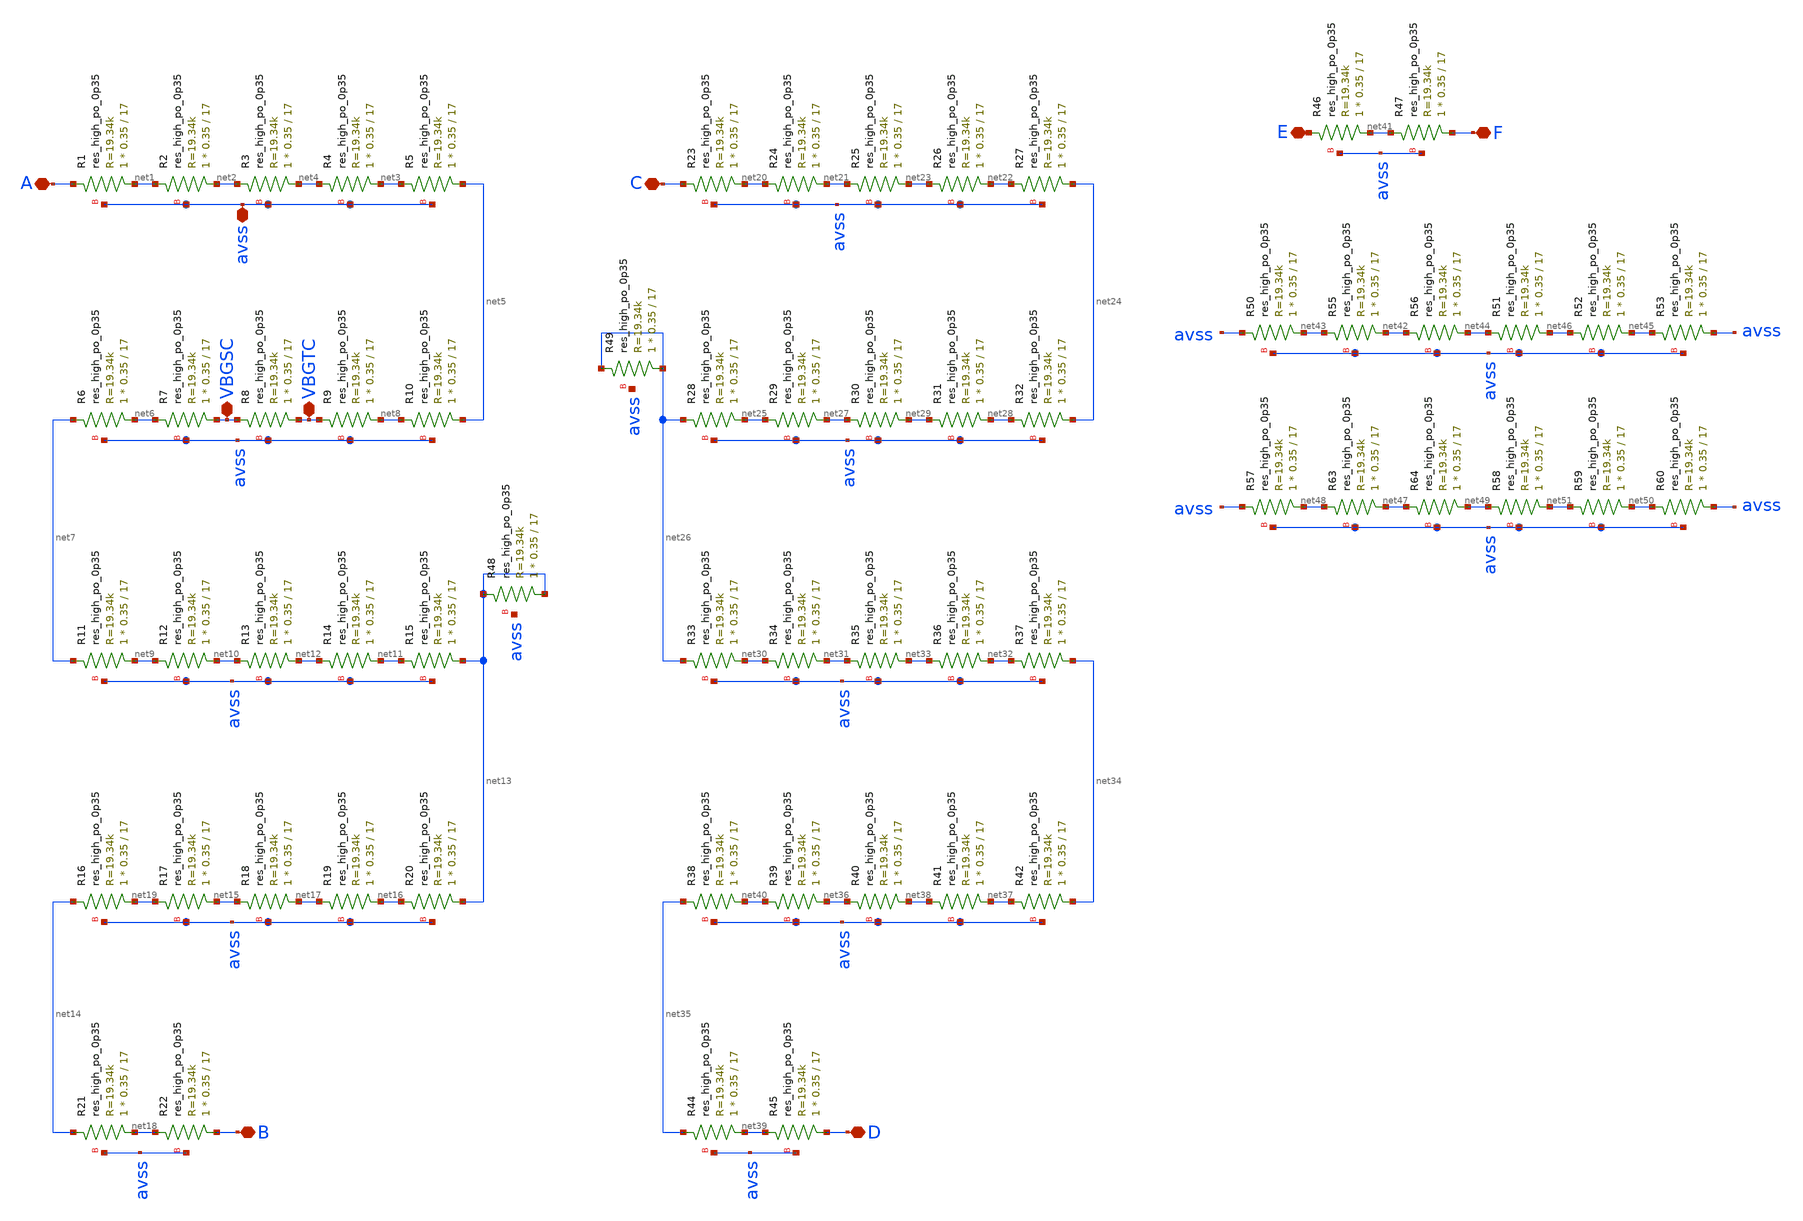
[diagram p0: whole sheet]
** sch_path: magic/resist_const.sch
**.subckt resist_const A VBGTC B VBGSC avss C D F E
*.iopin A
*.iopin VBGTC
*.iopin B
*.iopin VBGSC
*.iopin avss
*.iopin C
*.iopin D
*.iopin F
*.iopin E
XR1 net1 A avss sky130_fd_pr__res_high_po_0p35 L=17 mult=1 m=1
XR2 net2 net1 avss sky130_fd_pr__res_high_po_0p35 L=17 mult=1 m=1
XR3 net4 net2 avss sky130_fd_pr__res_high_po_0p35 L=17 mult=1 m=1
XR4 net3 net4 avss sky130_fd_pr__res_high_po_0p35 L=17 mult=1 m=1
XR5 net5 net3 avss sky130_fd_pr__res_high_po_0p35 L=17 mult=1 m=1
XR8 VBGTC VBGSC avss sky130_fd_pr__res_high_po_0p35 L=17 mult=1 m=1
XR9 net8 VBGTC avss sky130_fd_pr__res_high_po_0p35 L=17 mult=1 m=1
XR10 net5 net8 avss sky130_fd_pr__res_high_po_0p35 L=17 mult=1 m=1
XR12 net10 net9 avss sky130_fd_pr__res_high_po_0p35 L=17 mult=1 m=1
XR13 net12 net10 avss sky130_fd_pr__res_high_po_0p35 L=17 mult=1 m=1
XR14 net11 net12 avss sky130_fd_pr__res_high_po_0p35 L=17 mult=1 m=1
XR15 net13 net11 avss sky130_fd_pr__res_high_po_0p35 L=17 mult=1 m=1
XR17 net15 net19 avss sky130_fd_pr__res_high_po_0p35 L=17 mult=1 m=1
XR18 net17 net15 avss sky130_fd_pr__res_high_po_0p35 L=17 mult=1 m=1
XR19 net16 net17 avss sky130_fd_pr__res_high_po_0p35 L=17 mult=1 m=1
XR20 net13 net16 avss sky130_fd_pr__res_high_po_0p35 L=17 mult=1 m=1
XR22 B net18 avss sky130_fd_pr__res_high_po_0p35 L=17 mult=1 m=1
XR23 net20 C avss sky130_fd_pr__res_high_po_0p35 L=17 mult=1 m=1
XR24 net21 net20 avss sky130_fd_pr__res_high_po_0p35 L=17 mult=1 m=1
XR25 net23 net21 avss sky130_fd_pr__res_high_po_0p35 L=17 mult=1 m=1
XR26 net22 net23 avss sky130_fd_pr__res_high_po_0p35 L=17 mult=1 m=1
XR27 net24 net22 avss sky130_fd_pr__res_high_po_0p35 L=17 mult=1 m=1
XR30 net29 net27 avss sky130_fd_pr__res_high_po_0p35 L=17 mult=1 m=1
XR31 net28 net29 avss sky130_fd_pr__res_high_po_0p35 L=17 mult=1 m=1
XR32 net24 net28 avss sky130_fd_pr__res_high_po_0p35 L=17 mult=1 m=1
XR33 net30 net26 avss sky130_fd_pr__res_high_po_0p35 L=17 mult=1 m=1
XR34 net31 net30 avss sky130_fd_pr__res_high_po_0p35 L=17 mult=1 m=1
XR35 net33 net31 avss sky130_fd_pr__res_high_po_0p35 L=17 mult=1 m=1
XR36 net32 net33 avss sky130_fd_pr__res_high_po_0p35 L=17 mult=1 m=1
XR37 net34 net32 avss sky130_fd_pr__res_high_po_0p35 L=17 mult=1 m=1
XR39 net36 net40 avss sky130_fd_pr__res_high_po_0p35 L=17 mult=1 m=1
XR40 net38 net36 avss sky130_fd_pr__res_high_po_0p35 L=17 mult=1 m=1
XR41 net37 net38 avss sky130_fd_pr__res_high_po_0p35 L=17 mult=1 m=1
XR42 net34 net37 avss sky130_fd_pr__res_high_po_0p35 L=17 mult=1 m=1
XR44 net39 net35 avss sky130_fd_pr__res_high_po_0p35 L=17 mult=1 m=1
XR45 D net39 avss sky130_fd_pr__res_high_po_0p35 L=17 mult=1 m=1
XR46 net41 E avss sky130_fd_pr__res_high_po_0p35 L=17 mult=1 m=1
XR47 F net41 avss sky130_fd_pr__res_high_po_0p35 L=17 mult=1 m=1
XR28 net25 net26 avss sky130_fd_pr__res_high_po_0p35 L=17 mult=1 m=1
XR6 net6 net7 avss sky130_fd_pr__res_high_po_0p35 L=17 mult=1 m=1
XR16 net19 net14 avss sky130_fd_pr__res_high_po_0p35 L=17 mult=1 m=1
XR11 net9 net7 avss sky130_fd_pr__res_high_po_0p35 L=17 mult=1 m=1
XR21 net18 net14 avss sky130_fd_pr__res_high_po_0p35 L=17 mult=1 m=1
XR38 net40 net35 avss sky130_fd_pr__res_high_po_0p35 L=17 mult=1 m=1
XR29 net27 net25 avss sky130_fd_pr__res_high_po_0p35 L=17 mult=1 m=1
XR7 VBGSC net6 avss sky130_fd_pr__res_high_po_0p35 L=17 mult=1 m=1
XR48 net13 net13 avss sky130_fd_pr__res_high_po_0p35 L=17 mult=1 m=1
XR49 net26 net26 avss sky130_fd_pr__res_high_po_0p35 L=17 mult=1 m=1
XR50 net43 avss avss sky130_fd_pr__res_high_po_0p35 L=17 mult=1 m=1
XR51 net46 net44 avss sky130_fd_pr__res_high_po_0p35 L=17 mult=1 m=1
XR52 net45 net46 avss sky130_fd_pr__res_high_po_0p35 L=17 mult=1 m=1
XR53 avss net45 avss sky130_fd_pr__res_high_po_0p35 L=17 mult=1 m=1
XR55 net42 net43 avss sky130_fd_pr__res_high_po_0p35 L=17 mult=1 m=1
XR56 net44 net42 avss sky130_fd_pr__res_high_po_0p35 L=17 mult=1 m=1
XR57 net48 avss avss sky130_fd_pr__res_high_po_0p35 L=17 mult=1 m=1
XR58 net51 net49 avss sky130_fd_pr__res_high_po_0p35 L=17 mult=1 m=1
XR59 net50 net51 avss sky130_fd_pr__res_high_po_0p35 L=17 mult=1 m=1
XR60 avss net50 avss sky130_fd_pr__res_high_po_0p35 L=17 mult=1 m=1
XR63 net47 net48 avss sky130_fd_pr__res_high_po_0p35 L=17 mult=1 m=1
XR64 net49 net47 avss sky130_fd_pr__res_high_po_0p35 L=17 mult=1 m=1
**.ends
.end
